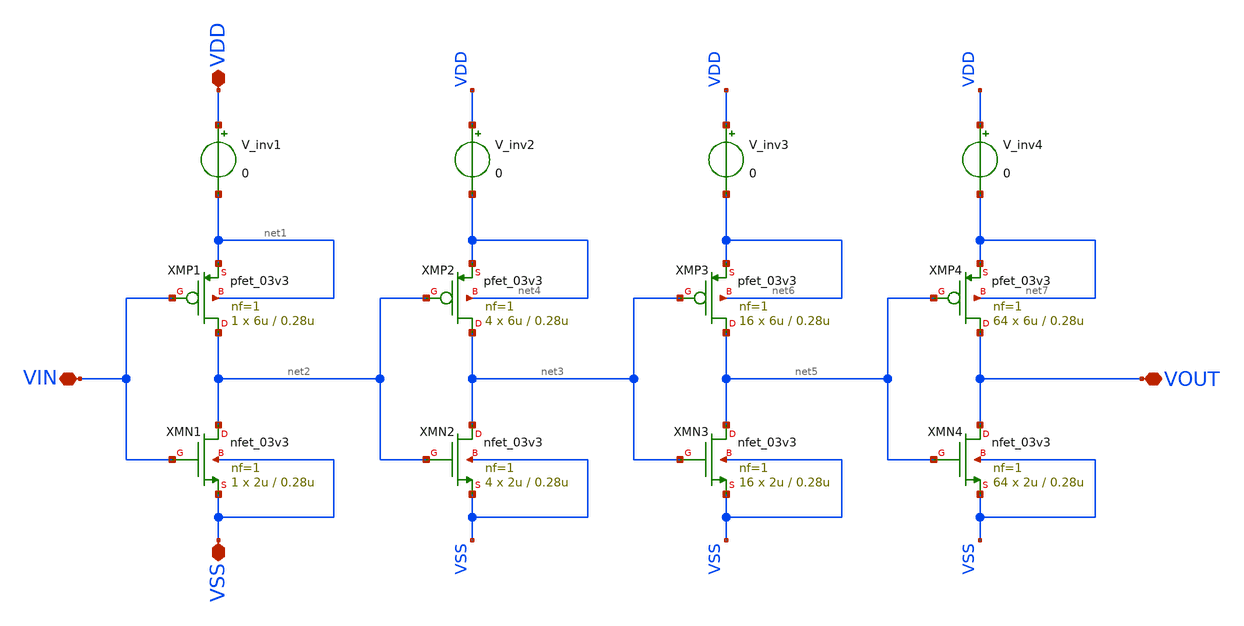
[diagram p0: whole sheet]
** sch_path: designs/sar_adc/digital/gate_buf_output/xschem/gate_buf_output.sch
**.subckt gate_buf_output VDD VSS VIN VOUT
*.iopin VDD
*.iopin VSS
*.iopin VIN
*.iopin VOUT
XMN1 net2 VIN VSS VSS nfet_03v3 L=0.28u W=2u nf=1 ad='int((nf+1)/2) * W/nf * 0.18u' as='int((nf+2)/2) * W/nf * 0.18u'
+ pd='2*int((nf+1)/2) * (W/nf + 0.18u)' ps='2*int((nf+2)/2) * (W/nf + 0.18u)' nrd='0.18u / W' nrs='0.18u / W'
+ sa=0 sb=0 sd=0 m=1
XMP1 net2 VIN net1 net1 pfet_03v3 L=0.28u W=6u nf=1 ad='int((nf+1)/2) * W/nf * 0.18u' as='int((nf+2)/2) * W/nf * 0.18u'
+ pd='2*int((nf+1)/2) * (W/nf + 0.18u)' ps='2*int((nf+2)/2) * (W/nf + 0.18u)' nrd='0.18u / W' nrs='0.18u / W'
+ sa=0 sb=0 sd=0 m=1
XMP2 net3 net2 net4 net4 pfet_03v3 L=0.28u W=6u nf=1 ad='int((nf+1)/2) * W/nf * 0.18u' as='int((nf+2)/2) * W/nf * 0.18u'
+ pd='2*int((nf+1)/2) * (W/nf + 0.18u)' ps='2*int((nf+2)/2) * (W/nf + 0.18u)' nrd='0.18u / W' nrs='0.18u / W'
+ sa=0 sb=0 sd=0 m=4
XMN2 net3 net2 VSS VSS nfet_03v3 L=0.28u W=2u nf=1 ad='int((nf+1)/2) * W/nf * 0.18u' as='int((nf+2)/2) * W/nf * 0.18u'
+ pd='2*int((nf+1)/2) * (W/nf + 0.18u)' ps='2*int((nf+2)/2) * (W/nf + 0.18u)' nrd='0.18u / W' nrs='0.18u / W'
+ sa=0 sb=0 sd=0 m=4
XMP3 net5 net3 net6 net6 pfet_03v3 L=0.28u W=6u nf=1 ad='int((nf+1)/2) * W/nf * 0.18u' as='int((nf+2)/2) * W/nf * 0.18u'
+ pd='2*int((nf+1)/2) * (W/nf + 0.18u)' ps='2*int((nf+2)/2) * (W/nf + 0.18u)' nrd='0.18u / W' nrs='0.18u / W'
+ sa=0 sb=0 sd=0 m=16
XMN3 net5 net3 VSS VSS nfet_03v3 L=0.28u W=2u nf=1 ad='int((nf+1)/2) * W/nf * 0.18u' as='int((nf+2)/2) * W/nf * 0.18u'
+ pd='2*int((nf+1)/2) * (W/nf + 0.18u)' ps='2*int((nf+2)/2) * (W/nf + 0.18u)' nrd='0.18u / W' nrs='0.18u / W'
+ sa=0 sb=0 sd=0 m=16
XMP4 VOUT net5 net7 net7 pfet_03v3 L=0.28u W=6u nf=1 ad='int((nf+1)/2) * W/nf * 0.18u' as='int((nf+2)/2) * W/nf * 0.18u'
+ pd='2*int((nf+1)/2) * (W/nf + 0.18u)' ps='2*int((nf+2)/2) * (W/nf + 0.18u)' nrd='0.18u / W' nrs='0.18u / W'
+ sa=0 sb=0 sd=0 m=64
XMN4 VOUT net5 VSS VSS nfet_03v3 L=0.28u W=2u nf=1 ad='int((nf+1)/2) * W/nf * 0.18u' as='int((nf+2)/2) * W/nf * 0.18u'
+ pd='2*int((nf+1)/2) * (W/nf + 0.18u)' ps='2*int((nf+2)/2) * (W/nf + 0.18u)' nrd='0.18u / W' nrs='0.18u / W'
+ sa=0 sb=0 sd=0 m=64
V_inv1 VDD net1 0
V_inv2 VDD net4 0
V_inv3 VDD net6 0
V_inv4 VDD net7 0
**.ends
.end
